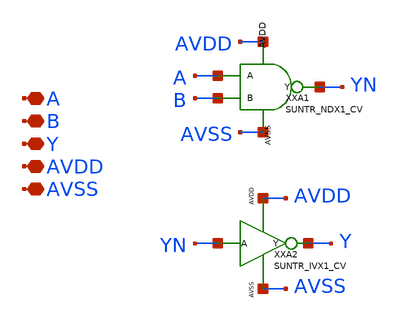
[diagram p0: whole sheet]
** sch_path: ip/sun_tr_sky130nm/design/SUN_TR_SKY130NM/SUNTR_ANX1_CV.sch
**.subckt SUNTR_ANX1_CV A B Y AVDD AVSS
*.iopin A
*.iopin B
*.iopin Y
*.iopin AVDD
*.iopin AVSS
XXA1 AVSS AVDD B A YN SUNTR_NDX1_CV
XXA2 YN Y AVDD AVSS SUNTR_IVX1_CV
**.ends
.end
